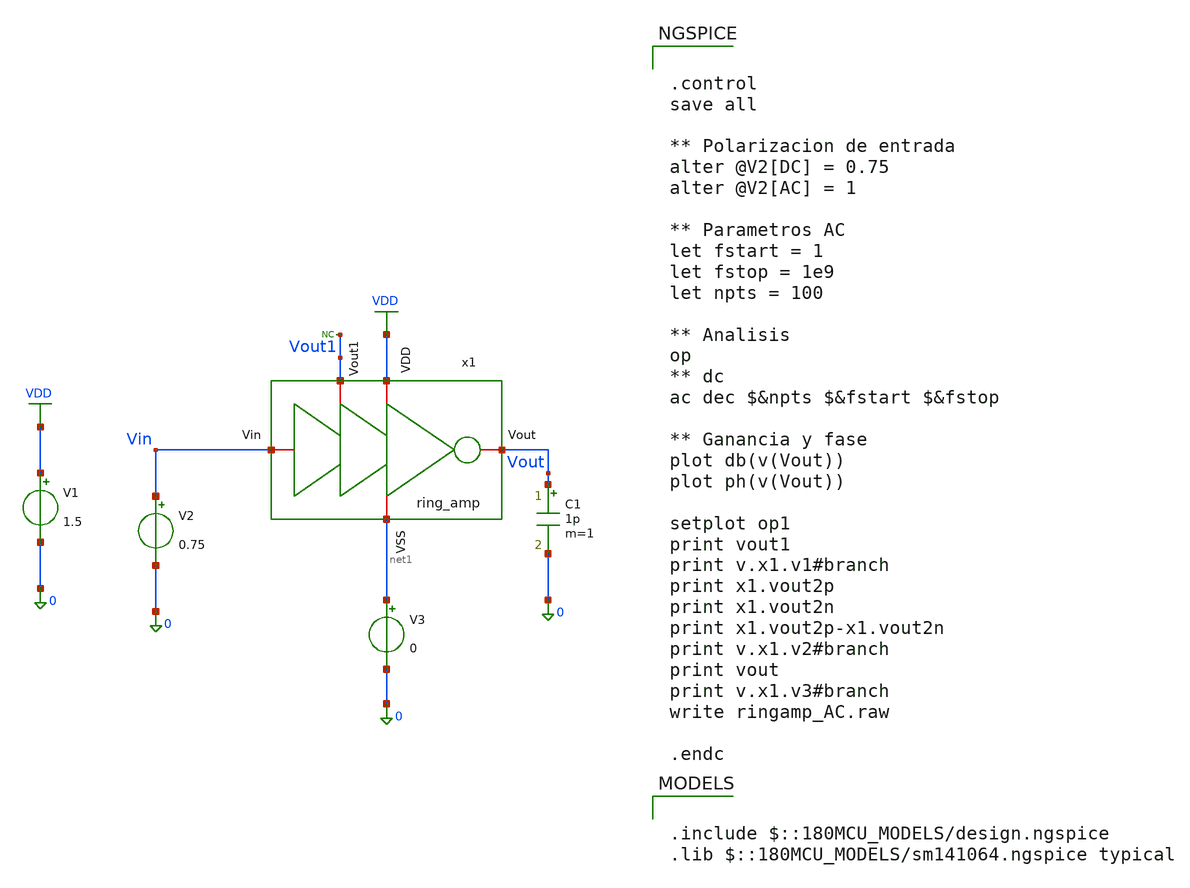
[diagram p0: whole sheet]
** sch_path: designs/DS_modulator/ring_amp/xschem/ring_amp_TB_AC.sch
**.subckt ring_amp_TB_AC
C1 Vout 0 1p m=1
* noconn Vout1
V1 VDD 0 1.5
V2 Vin 0 0.75
x1 VDD Vin Vout Vout1 net1 ring_amp
V3 net1 0 0
**** begin user architecture code

.include $::180MCU_MODELS/design.ngspice
.lib $::180MCU_MODELS/sm141064.ngspice typical



.control
save all

** Polarizacion de entrada
alter @V2[DC] = 0.75
alter @V2[AC] = 1

** Parametros AC
let fstart = 1
let fstop = 1e9
let npts = 100

** Analisis
op
** dc
ac dec $&npts $&fstart $&fstop

** Ganancia y fase
plot db(v(Vout))
plot ph(v(Vout))

setplot op1
print vout1
print v.x1.v1#branch
print x1.vout2p
print x1.vout2n
print x1.vout2p-x1.vout2n
print v.x1.v2#branch
print vout
print v.x1.v3#branch
write ringamp_AC.raw

.endc


**** end user architecture code
**.ends
.GLOBAL VDD
.end
